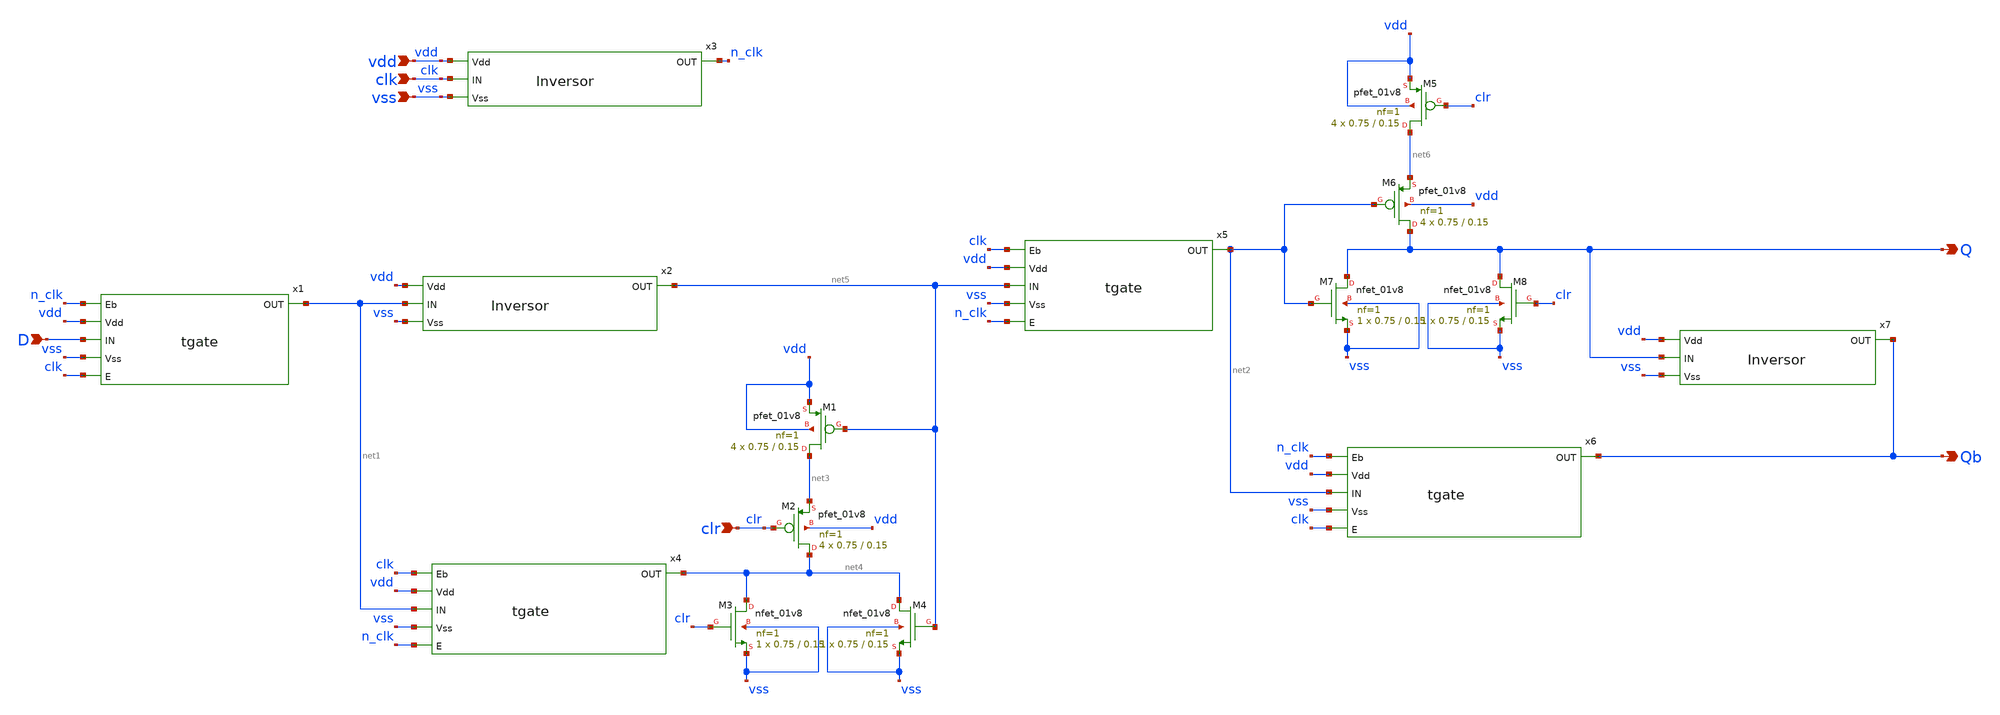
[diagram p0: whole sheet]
** sch_path: icdesign/sch/FFD/ffd.sch
**.subckt ffd clk vdd vss D clr Q Qb
*.ipin clk
*.ipin vdd
*.ipin vss
*.ipin D
*.ipin clr
*.opin Q
*.opin Qb
x1 n_clk vdd D net1 vss clk tgate
x2 vdd net1 net5 vss Inversor
x3 vdd clk n_clk vss Inversor
x4 clk vdd net1 net4 vss n_clk tgate
x5 clk vdd net5 net2 vss n_clk tgate
x6 n_clk vdd net2 Qb vss clk tgate
x7 vdd Q Qb vss Inversor
XM1 net3 net5 vdd vdd sky130_fd_pr__pfet_01v8 L=0.15 W=0.75 nf=1 ad='int((nf+1)/2) * W/nf * 0.29' as='int((nf+2)/2) * W/nf * 0.29'
+ pd='2*int((nf+1)/2) * (W/nf + 0.29)' ps='2*int((nf+2)/2) * (W/nf + 0.29)' nrd='0.29 / W' nrs='0.29 / W'
+ sa=0 sb=0 sd=0 mult=4 m=4
XM2 net4 clr net3 vdd sky130_fd_pr__pfet_01v8 L=0.15 W=0.75 nf=1 ad='int((nf+1)/2) * W/nf * 0.29' as='int((nf+2)/2) * W/nf * 0.29'
+ pd='2*int((nf+1)/2) * (W/nf + 0.29)' ps='2*int((nf+2)/2) * (W/nf + 0.29)' nrd='0.29 / W' nrs='0.29 / W'
+ sa=0 sb=0 sd=0 mult=4 m=4
XM3 net4 clr vss vss sky130_fd_pr__nfet_01v8 L=0.15 W=0.75 nf=1 ad='int((nf+1)/2) * W/nf * 0.29' as='int((nf+2)/2) * W/nf * 0.29'
+ pd='2*int((nf+1)/2) * (W/nf + 0.29)' ps='2*int((nf+2)/2) * (W/nf + 0.29)' nrd='0.29 / W' nrs='0.29 / W'
+ sa=0 sb=0 sd=0 mult=1 m=1
XM4 net4 net5 vss vss sky130_fd_pr__nfet_01v8 L=0.15 W=0.75 nf=1 ad='int((nf+1)/2) * W/nf * 0.29' as='int((nf+2)/2) * W/nf * 0.29'
+ pd='2*int((nf+1)/2) * (W/nf + 0.29)' ps='2*int((nf+2)/2) * (W/nf + 0.29)' nrd='0.29 / W' nrs='0.29 / W'
+ sa=0 sb=0 sd=0 mult=1 m=1
XM5 net6 clr vdd vdd sky130_fd_pr__pfet_01v8 L=0.15 W=0.75 nf=1 ad='int((nf+1)/2) * W/nf * 0.29' as='int((nf+2)/2) * W/nf * 0.29'
+ pd='2*int((nf+1)/2) * (W/nf + 0.29)' ps='2*int((nf+2)/2) * (W/nf + 0.29)' nrd='0.29 / W' nrs='0.29 / W'
+ sa=0 sb=0 sd=0 mult=4 m=4
XM6 Q net2 net6 vdd sky130_fd_pr__pfet_01v8 L=0.15 W=0.75 nf=1 ad='int((nf+1)/2) * W/nf * 0.29' as='int((nf+2)/2) * W/nf * 0.29'
+ pd='2*int((nf+1)/2) * (W/nf + 0.29)' ps='2*int((nf+2)/2) * (W/nf + 0.29)' nrd='0.29 / W' nrs='0.29 / W'
+ sa=0 sb=0 sd=0 mult=4 m=4
XM7 Q net2 vss vss sky130_fd_pr__nfet_01v8 L=0.15 W=0.75 nf=1 ad='int((nf+1)/2) * W/nf * 0.29' as='int((nf+2)/2) * W/nf * 0.29'
+ pd='2*int((nf+1)/2) * (W/nf + 0.29)' ps='2*int((nf+2)/2) * (W/nf + 0.29)' nrd='0.29 / W' nrs='0.29 / W'
+ sa=0 sb=0 sd=0 mult=1 m=1
XM8 Q clr vss vss sky130_fd_pr__nfet_01v8 L=0.15 W=0.75 nf=1 ad='int((nf+1)/2) * W/nf * 0.29' as='int((nf+2)/2) * W/nf * 0.29'
+ pd='2*int((nf+1)/2) * (W/nf + 0.29)' ps='2*int((nf+2)/2) * (W/nf + 0.29)' nrd='0.29 / W' nrs='0.29 / W'
+ sa=0 sb=0 sd=0 mult=1 m=1
**.ends

* expanding   symbol:  TGate/tgate.sym # of pins=6
** sym_path: icdesign/sch/TGate/tgate.sym
** sch_path: icdesign/sch/TGate/tgate.sch
.subckt tgate Eb Vdd IN OUT Vss E
*.opin OUT
*.ipin IN
*.ipin Eb
*.ipin E
*.ipin Vdd
*.ipin Vss
XM1 IN E OUT Vss sky130_fd_pr__nfet_01v8 L=0.15 W=0.75 nf=1 ad='int((nf+1)/2) * W/nf * 0.29' as='int((nf+2)/2) * W/nf * 0.29'
+ pd='2*int((nf+1)/2) * (W/nf + 0.29)' ps='2*int((nf+2)/2) * (W/nf + 0.29)' nrd='0.29 / W' nrs='0.29 / W'
+ sa=0 sb=0 sd=0 mult=1 m=1
XM2 IN Eb OUT Vdd sky130_fd_pr__pfet_01v8 L=0.15 W=0.75 nf=1 ad='int((nf+1)/2) * W/nf * 0.29' as='int((nf+2)/2) * W/nf * 0.29'
+ pd='2*int((nf+1)/2) * (W/nf + 0.29)' ps='2*int((nf+2)/2) * (W/nf + 0.29)' nrd='0.29 / W' nrs='0.29 / W'
+ sa=0 sb=0 sd=0 mult=2 m=2
.ends


* expanding   symbol:  Inversor/Inversor.sym # of pins=4
** sym_path: icdesign/sch/Inversor/Inversor.sym
** sch_path: icdesign/sch/Inversor/Inversor.sch
.subckt Inversor Vdd IN OUT Vss
*.ipin IN
*.ipin Vdd
*.ipin Vss
*.opin OUT
XM1 OUT IN Vss Vss sky130_fd_pr__nfet_01v8 L=0.15 W=0.75 nf=1 ad='int((nf+1)/2) * W/nf * 0.29' as='int((nf+2)/2) * W/nf * 0.29'
+ pd='2*int((nf+1)/2) * (W/nf + 0.29)' ps='2*int((nf+2)/2) * (W/nf + 0.29)' nrd='0.29 / W' nrs='0.29 / W'
+ sa=0 sb=0 sd=0 mult=1 m=1
XM2 OUT IN Vdd Vdd sky130_fd_pr__pfet_01v8 L=0.15 W=0.75 nf=1 ad='int((nf+1)/2) * W/nf * 0.29' as='int((nf+2)/2) * W/nf * 0.29'
+ pd='2*int((nf+1)/2) * (W/nf + 0.29)' ps='2*int((nf+2)/2) * (W/nf + 0.29)' nrd='0.29 / W' nrs='0.29 / W'
+ sa=0 sb=0 sd=0 mult=2 m=2
.ends

.end
